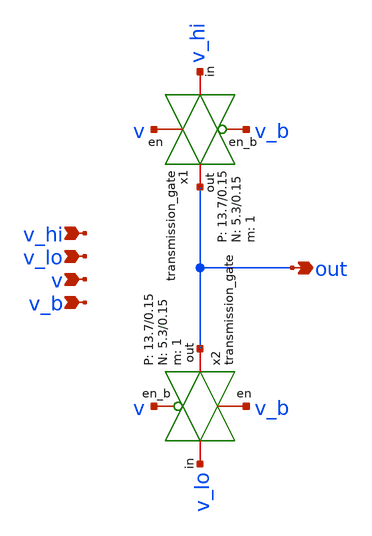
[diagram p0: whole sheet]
** sch_path: design/schematic/1b_dac.sch
**.subckt 1b_dac v_hi v_lo v v_b out
*.ipin v_hi
*.ipin v_lo
*.ipin v
*.ipin v_b
*.opin out
x1 v_hi out v v_b VDD VSS 1 5.3 0.15 13.7 0.15 transmission_gate
x2 v_lo out v_b v VDD VSS 1 5.3 0.15 13.7 0.15 transmission_gate
**.ends

* expanding   symbol:  transmission_gate.sym # of pins=4
** sym_path: design/schematic/transmission_gate.sym
** sch_path: design/schematic/transmission_gate.sch
.subckt transmission_gate in out en en_b VDD VSS N W_N L_N W_P L_P    N=1 W_N=5.3 L_N=0.15 W_P=13.7
+ L_P=0.15
*.iopin in
*.iopin out
*.ipin en
*.ipin en_b
XM1 out en in VSS sky130_fd_pr__nfet_01v8 L=L_N W=W_N nf=1 ad='int((nf+1)/2) * W/nf * 0.29' as='int((nf+2)/2) * W/nf * 0.29'
+ pd='2*int((nf+1)/2) * (W/nf + 0.29)' ps='2*int((nf+2)/2) * (W/nf + 0.29)' nrd='0.29 / W' nrs='0.29 / W'
+ sa=0 sb=0 sd=0 mult=N m=N
XM2 out en_b in VDD sky130_fd_pr__pfet_01v8 L=L_P W=W_P nf=1 ad='int((nf+1)/2) * W/nf * 0.29' as='int((nf+2)/2) * W/nf * 0.29'
+ pd='2*int((nf+1)/2) * (W/nf + 0.29)' ps='2*int((nf+2)/2) * (W/nf + 0.29)' nrd='0.29 / W' nrs='0.29 / W'
+ sa=0 sb=0 sd=0 mult=N m=N
.ends

.end
